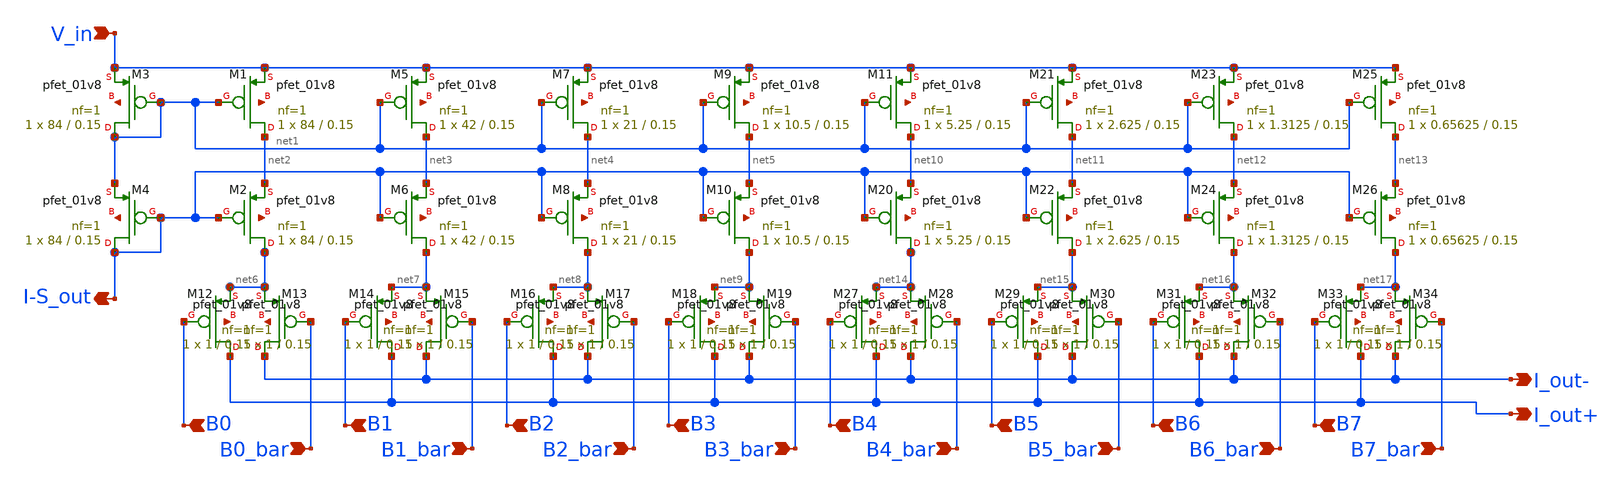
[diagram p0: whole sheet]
** sch_path: analog/schematics/DAC.sch
**.subckt DAC I-S_out B0 V_in B0_bar B1 B2 B3 B1_bar B2_bar B3_bar B4 B4_bar B5 B6 B7 B5_bar B6_bar
*+ B7_bar I_out+ I_out-
*.opin I-S_out
*.ipin B0
*.ipin V_in
*.ipin B0_bar
*.ipin B1
*.ipin B2
*.ipin B3
*.ipin B1_bar
*.ipin B2_bar
*.ipin B3_bar
*.ipin B4
*.ipin B4_bar
*.ipin B5
*.ipin B6
*.ipin B7
*.ipin B5_bar
*.ipin B6_bar
*.ipin B7_bar
*.opin I_out+
*.opin I_out-
XM1 net2 net1 V_in net18 sky130_fd_pr__pfet_01v8 L=0.15 W=84 nf=1 ad='int((nf+1)/2) * W/nf * 0.29' as='int((nf+2)/2) * W/nf * 0.29'
+ pd='2*int((nf+1)/2) * (W/nf + 0.29)' ps='2*int((nf+2)/2) * (W/nf + 0.29)' nrd='0.29 / W' nrs='0.29 / W'
+ sa=0 sb=0 sd=0 mult=1 m=1
XM2 net6 I-S_out net2 net19 sky130_fd_pr__pfet_01v8 L=0.15 W=84 nf=1 ad='int((nf+1)/2) * W/nf * 0.29'
+ as='int((nf+2)/2) * W/nf * 0.29' pd='2*int((nf+1)/2) * (W/nf + 0.29)' ps='2*int((nf+2)/2) * (W/nf + 0.29)'
+ nrd='0.29 / W' nrs='0.29 / W' sa=0 sb=0 sd=0 mult=1 m=1
XM3 net1 net1 V_in net20 sky130_fd_pr__pfet_01v8 L=0.15 W=84 nf=1 ad='int((nf+1)/2) * W/nf * 0.29' as='int((nf+2)/2) * W/nf * 0.29'
+ pd='2*int((nf+1)/2) * (W/nf + 0.29)' ps='2*int((nf+2)/2) * (W/nf + 0.29)' nrd='0.29 / W' nrs='0.29 / W'
+ sa=0 sb=0 sd=0 mult=1 m=1
XM4 I-S_out I-S_out net1 net21 sky130_fd_pr__pfet_01v8 L=0.15 W=84 nf=1 ad='int((nf+1)/2) * W/nf * 0.29'
+ as='int((nf+2)/2) * W/nf * 0.29' pd='2*int((nf+1)/2) * (W/nf + 0.29)' ps='2*int((nf+2)/2) * (W/nf + 0.29)'
+ nrd='0.29 / W' nrs='0.29 / W' sa=0 sb=0 sd=0 mult=1 m=1
XM5 net3 net1 V_in net22 sky130_fd_pr__pfet_01v8 L=0.15 W=42 nf=1 ad='int((nf+1)/2) * W/nf * 0.29' as='int((nf+2)/2) * W/nf * 0.29'
+ pd='2*int((nf+1)/2) * (W/nf + 0.29)' ps='2*int((nf+2)/2) * (W/nf + 0.29)' nrd='0.29 / W' nrs='0.29 / W'
+ sa=0 sb=0 sd=0 mult=1 m=1
XM6 net7 I-S_out net3 net23 sky130_fd_pr__pfet_01v8 L=0.15 W=42 nf=1 ad='int((nf+1)/2) * W/nf * 0.29'
+ as='int((nf+2)/2) * W/nf * 0.29' pd='2*int((nf+1)/2) * (W/nf + 0.29)' ps='2*int((nf+2)/2) * (W/nf + 0.29)'
+ nrd='0.29 / W' nrs='0.29 / W' sa=0 sb=0 sd=0 mult=1 m=1
XM7 net4 net1 V_in net24 sky130_fd_pr__pfet_01v8 L=0.15 W=21 nf=1 ad='int((nf+1)/2) * W/nf * 0.29' as='int((nf+2)/2) * W/nf * 0.29'
+ pd='2*int((nf+1)/2) * (W/nf + 0.29)' ps='2*int((nf+2)/2) * (W/nf + 0.29)' nrd='0.29 / W' nrs='0.29 / W'
+ sa=0 sb=0 sd=0 mult=1 m=1
XM8 net8 I-S_out net4 net25 sky130_fd_pr__pfet_01v8 L=0.15 W=21 nf=1 ad='int((nf+1)/2) * W/nf * 0.29'
+ as='int((nf+2)/2) * W/nf * 0.29' pd='2*int((nf+1)/2) * (W/nf + 0.29)' ps='2*int((nf+2)/2) * (W/nf + 0.29)'
+ nrd='0.29 / W' nrs='0.29 / W' sa=0 sb=0 sd=0 mult=1 m=1
XM9 net5 net1 V_in net26 sky130_fd_pr__pfet_01v8 L=0.15 W=10.5 nf=1 ad='int((nf+1)/2) * W/nf * 0.29'
+ as='int((nf+2)/2) * W/nf * 0.29' pd='2*int((nf+1)/2) * (W/nf + 0.29)' ps='2*int((nf+2)/2) * (W/nf + 0.29)'
+ nrd='0.29 / W' nrs='0.29 / W' sa=0 sb=0 sd=0 mult=1 m=1
XM10 net9 I-S_out net5 net27 sky130_fd_pr__pfet_01v8 L=0.15 W=10.5 nf=1 ad='int((nf+1)/2) * W/nf * 0.29'
+ as='int((nf+2)/2) * W/nf * 0.29' pd='2*int((nf+1)/2) * (W/nf + 0.29)' ps='2*int((nf+2)/2) * (W/nf + 0.29)'
+ nrd='0.29 / W' nrs='0.29 / W' sa=0 sb=0 sd=0 mult=1 m=1
XM12 I_out+ B0 net6 net28 sky130_fd_pr__pfet_01v8 L=0.15 W=1 nf=1 ad='int((nf+1)/2) * W/nf * 0.29' as='int((nf+2)/2) * W/nf * 0.29'
+ pd='2*int((nf+1)/2) * (W/nf + 0.29)' ps='2*int((nf+2)/2) * (W/nf + 0.29)' nrd='0.29 / W' nrs='0.29 / W'
+ sa=0 sb=0 sd=0 mult=1 m=1
XM13 I_out- B0_bar net6 net29 sky130_fd_pr__pfet_01v8 L=0.15 W=1 nf=1 ad='int((nf+1)/2) * W/nf * 0.29'
+ as='int((nf+2)/2) * W/nf * 0.29' pd='2*int((nf+1)/2) * (W/nf + 0.29)' ps='2*int((nf+2)/2) * (W/nf + 0.29)'
+ nrd='0.29 / W' nrs='0.29 / W' sa=0 sb=0 sd=0 mult=1 m=1
XM14 I_out+ B1 net7 net30 sky130_fd_pr__pfet_01v8 L=0.15 W=1 nf=1 ad='int((nf+1)/2) * W/nf * 0.29' as='int((nf+2)/2) * W/nf * 0.29'
+ pd='2*int((nf+1)/2) * (W/nf + 0.29)' ps='2*int((nf+2)/2) * (W/nf + 0.29)' nrd='0.29 / W' nrs='0.29 / W'
+ sa=0 sb=0 sd=0 mult=1 m=1
XM15 I_out- B1_bar net7 net31 sky130_fd_pr__pfet_01v8 L=0.15 W=1 nf=1 ad='int((nf+1)/2) * W/nf * 0.29'
+ as='int((nf+2)/2) * W/nf * 0.29' pd='2*int((nf+1)/2) * (W/nf + 0.29)' ps='2*int((nf+2)/2) * (W/nf + 0.29)'
+ nrd='0.29 / W' nrs='0.29 / W' sa=0 sb=0 sd=0 mult=1 m=1
XM16 I_out+ B2 net8 net32 sky130_fd_pr__pfet_01v8 L=0.15 W=1 nf=1 ad='int((nf+1)/2) * W/nf * 0.29' as='int((nf+2)/2) * W/nf * 0.29'
+ pd='2*int((nf+1)/2) * (W/nf + 0.29)' ps='2*int((nf+2)/2) * (W/nf + 0.29)' nrd='0.29 / W' nrs='0.29 / W'
+ sa=0 sb=0 sd=0 mult=1 m=1
XM17 I_out- B2_bar net8 net33 sky130_fd_pr__pfet_01v8 L=0.15 W=1 nf=1 ad='int((nf+1)/2) * W/nf * 0.29'
+ as='int((nf+2)/2) * W/nf * 0.29' pd='2*int((nf+1)/2) * (W/nf + 0.29)' ps='2*int((nf+2)/2) * (W/nf + 0.29)'
+ nrd='0.29 / W' nrs='0.29 / W' sa=0 sb=0 sd=0 mult=1 m=1
XM18 I_out+ B3 net9 net34 sky130_fd_pr__pfet_01v8 L=0.15 W=1 nf=1 ad='int((nf+1)/2) * W/nf * 0.29' as='int((nf+2)/2) * W/nf * 0.29'
+ pd='2*int((nf+1)/2) * (W/nf + 0.29)' ps='2*int((nf+2)/2) * (W/nf + 0.29)' nrd='0.29 / W' nrs='0.29 / W'
+ sa=0 sb=0 sd=0 mult=1 m=1
XM19 I_out- B3_bar net9 net35 sky130_fd_pr__pfet_01v8 L=0.15 W=1 nf=1 ad='int((nf+1)/2) * W/nf * 0.29'
+ as='int((nf+2)/2) * W/nf * 0.29' pd='2*int((nf+1)/2) * (W/nf + 0.29)' ps='2*int((nf+2)/2) * (W/nf + 0.29)'
+ nrd='0.29 / W' nrs='0.29 / W' sa=0 sb=0 sd=0 mult=1 m=1
XM11 net10 net1 V_in net36 sky130_fd_pr__pfet_01v8 L=0.15 W=5.25 nf=1 ad='int((nf+1)/2) * W/nf * 0.29'
+ as='int((nf+2)/2) * W/nf * 0.29' pd='2*int((nf+1)/2) * (W/nf + 0.29)' ps='2*int((nf+2)/2) * (W/nf + 0.29)'
+ nrd='0.29 / W' nrs='0.29 / W' sa=0 sb=0 sd=0 mult=1 m=1
XM20 net14 I-S_out net10 net37 sky130_fd_pr__pfet_01v8 L=0.15 W=5.25 nf=1 ad='int((nf+1)/2) * W/nf * 0.29'
+ as='int((nf+2)/2) * W/nf * 0.29' pd='2*int((nf+1)/2) * (W/nf + 0.29)' ps='2*int((nf+2)/2) * (W/nf + 0.29)'
+ nrd='0.29 / W' nrs='0.29 / W' sa=0 sb=0 sd=0 mult=1 m=1
XM21 net11 net1 V_in net38 sky130_fd_pr__pfet_01v8 L=0.15 W=2.625 nf=1 ad='int((nf+1)/2) * W/nf * 0.29'
+ as='int((nf+2)/2) * W/nf * 0.29' pd='2*int((nf+1)/2) * (W/nf + 0.29)' ps='2*int((nf+2)/2) * (W/nf + 0.29)'
+ nrd='0.29 / W' nrs='0.29 / W' sa=0 sb=0 sd=0 mult=1 m=1
XM22 net15 I-S_out net11 net39 sky130_fd_pr__pfet_01v8 L=0.15 W=2.625 nf=1 ad='int((nf+1)/2) * W/nf * 0.29'
+ as='int((nf+2)/2) * W/nf * 0.29' pd='2*int((nf+1)/2) * (W/nf + 0.29)' ps='2*int((nf+2)/2) * (W/nf + 0.29)'
+ nrd='0.29 / W' nrs='0.29 / W' sa=0 sb=0 sd=0 mult=1 m=1
XM23 net12 net1 V_in net40 sky130_fd_pr__pfet_01v8 L=0.15 W=1.3125 nf=1 ad='int((nf+1)/2) * W/nf * 0.29'
+ as='int((nf+2)/2) * W/nf * 0.29' pd='2*int((nf+1)/2) * (W/nf + 0.29)' ps='2*int((nf+2)/2) * (W/nf + 0.29)'
+ nrd='0.29 / W' nrs='0.29 / W' sa=0 sb=0 sd=0 mult=1 m=1
XM24 net16 I-S_out net12 net41 sky130_fd_pr__pfet_01v8 L=0.15 W=1.3125 nf=1 ad='int((nf+1)/2) * W/nf * 0.29'
+ as='int((nf+2)/2) * W/nf * 0.29' pd='2*int((nf+1)/2) * (W/nf + 0.29)' ps='2*int((nf+2)/2) * (W/nf + 0.29)'
+ nrd='0.29 / W' nrs='0.29 / W' sa=0 sb=0 sd=0 mult=1 m=1
XM25 net13 net1 V_in net42 sky130_fd_pr__pfet_01v8 L=0.15 W=0.65625 nf=1 ad='int((nf+1)/2) * W/nf * 0.29'
+ as='int((nf+2)/2) * W/nf * 0.29' pd='2*int((nf+1)/2) * (W/nf + 0.29)' ps='2*int((nf+2)/2) * (W/nf + 0.29)'
+ nrd='0.29 / W' nrs='0.29 / W' sa=0 sb=0 sd=0 mult=1 m=1
XM26 net17 I-S_out net13 net43 sky130_fd_pr__pfet_01v8 L=0.15 W=0.65625 nf=1 ad='int((nf+1)/2) * W/nf * 0.29'
+ as='int((nf+2)/2) * W/nf * 0.29' pd='2*int((nf+1)/2) * (W/nf + 0.29)' ps='2*int((nf+2)/2) * (W/nf + 0.29)'
+ nrd='0.29 / W' nrs='0.29 / W' sa=0 sb=0 sd=0 mult=1 m=1
XM27 I_out+ B4 net14 net44 sky130_fd_pr__pfet_01v8 L=0.15 W=1 nf=1 ad='int((nf+1)/2) * W/nf * 0.29' as='int((nf+2)/2) * W/nf * 0.29'
+ pd='2*int((nf+1)/2) * (W/nf + 0.29)' ps='2*int((nf+2)/2) * (W/nf + 0.29)' nrd='0.29 / W' nrs='0.29 / W'
+ sa=0 sb=0 sd=0 mult=1 m=1
XM28 I_out- B4_bar net14 net45 sky130_fd_pr__pfet_01v8 L=0.15 W=1 nf=1 ad='int((nf+1)/2) * W/nf * 0.29'
+ as='int((nf+2)/2) * W/nf * 0.29' pd='2*int((nf+1)/2) * (W/nf + 0.29)' ps='2*int((nf+2)/2) * (W/nf + 0.29)'
+ nrd='0.29 / W' nrs='0.29 / W' sa=0 sb=0 sd=0 mult=1 m=1
XM29 I_out+ B5 net15 net46 sky130_fd_pr__pfet_01v8 L=0.15 W=1 nf=1 ad='int((nf+1)/2) * W/nf * 0.29' as='int((nf+2)/2) * W/nf * 0.29'
+ pd='2*int((nf+1)/2) * (W/nf + 0.29)' ps='2*int((nf+2)/2) * (W/nf + 0.29)' nrd='0.29 / W' nrs='0.29 / W'
+ sa=0 sb=0 sd=0 mult=1 m=1
XM30 I_out- B5_bar net15 net47 sky130_fd_pr__pfet_01v8 L=0.15 W=1 nf=1 ad='int((nf+1)/2) * W/nf * 0.29'
+ as='int((nf+2)/2) * W/nf * 0.29' pd='2*int((nf+1)/2) * (W/nf + 0.29)' ps='2*int((nf+2)/2) * (W/nf + 0.29)'
+ nrd='0.29 / W' nrs='0.29 / W' sa=0 sb=0 sd=0 mult=1 m=1
XM31 I_out+ B6 net16 net48 sky130_fd_pr__pfet_01v8 L=0.15 W=1 nf=1 ad='int((nf+1)/2) * W/nf * 0.29' as='int((nf+2)/2) * W/nf * 0.29'
+ pd='2*int((nf+1)/2) * (W/nf + 0.29)' ps='2*int((nf+2)/2) * (W/nf + 0.29)' nrd='0.29 / W' nrs='0.29 / W'
+ sa=0 sb=0 sd=0 mult=1 m=1
XM32 I_out- B6_bar net16 net49 sky130_fd_pr__pfet_01v8 L=0.15 W=1 nf=1 ad='int((nf+1)/2) * W/nf * 0.29'
+ as='int((nf+2)/2) * W/nf * 0.29' pd='2*int((nf+1)/2) * (W/nf + 0.29)' ps='2*int((nf+2)/2) * (W/nf + 0.29)'
+ nrd='0.29 / W' nrs='0.29 / W' sa=0 sb=0 sd=0 mult=1 m=1
XM33 I_out+ B7 net17 net50 sky130_fd_pr__pfet_01v8 L=0.15 W=1 nf=1 ad='int((nf+1)/2) * W/nf * 0.29' as='int((nf+2)/2) * W/nf * 0.29'
+ pd='2*int((nf+1)/2) * (W/nf + 0.29)' ps='2*int((nf+2)/2) * (W/nf + 0.29)' nrd='0.29 / W' nrs='0.29 / W'
+ sa=0 sb=0 sd=0 mult=1 m=1
XM34 I_out- B7_bar net17 net51 sky130_fd_pr__pfet_01v8 L=0.15 W=1 nf=1 ad='int((nf+1)/2) * W/nf * 0.29'
+ as='int((nf+2)/2) * W/nf * 0.29' pd='2*int((nf+1)/2) * (W/nf + 0.29)' ps='2*int((nf+2)/2) * (W/nf + 0.29)'
+ nrd='0.29 / W' nrs='0.29 / W' sa=0 sb=0 sd=0 mult=1 m=1
**.ends
.end
